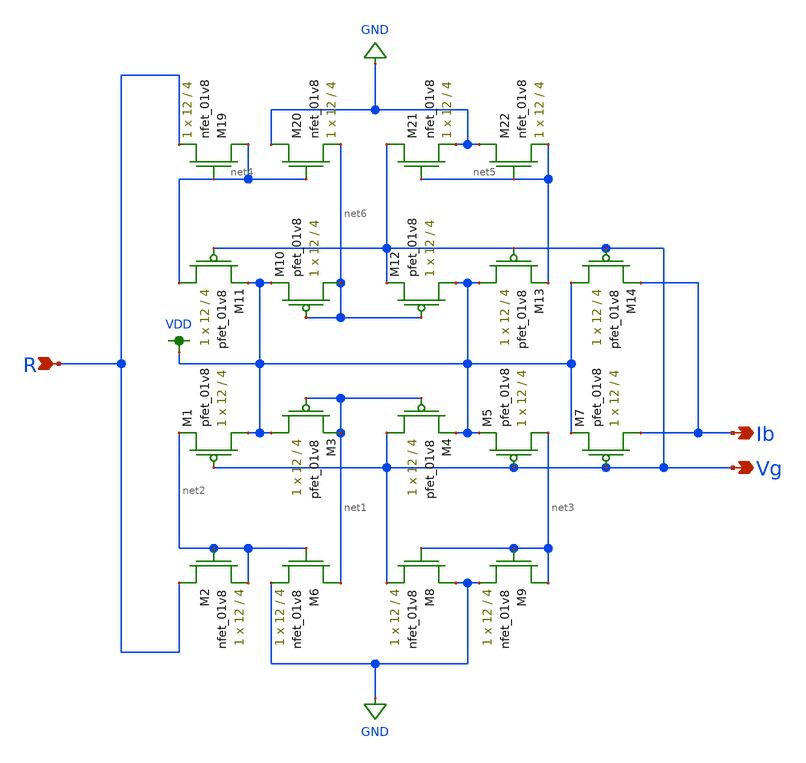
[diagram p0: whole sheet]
** sch_path: modules/bias_gen_lds.sch
**.subckt bias_gen_lds R Ib Vg
*.ipin R
*.opin Ib
*.opin Vg
XM2 R net2 net2 GND sky130_fd_pr__nfet_01v8 L=4 W=12 nf=1 ad='int((nf+1)/2) * W/nf * 0.29' as='int((nf+2)/2) * W/nf * 0.29'
+ pd='2*int((nf+1)/2) * (W/nf + 0.29)' ps='2*int((nf+2)/2) * (W/nf + 0.29)' nrd='0.29 / W' nrs='0.29 / W'
+ sa=0 sb=0 sd=0 mult=1 m=1
XM3 VDD net1 net1 VDD sky130_fd_pr__pfet_01v8 L=4 W=12 nf=1 ad='int((nf+1)/2) * W/nf * 0.29' as='int((nf+2)/2) * W/nf * 0.29'
+ pd='2*int((nf+1)/2) * (W/nf + 0.29)' ps='2*int((nf+2)/2) * (W/nf + 0.29)' nrd='0.29 / W' nrs='0.29 / W'
+ sa=0 sb=0 sd=0 mult=1 m=1
XM1 VDD Vg net2 VDD sky130_fd_pr__pfet_01v8 L=4 W=12 nf=1 ad='int((nf+1)/2) * W/nf * 0.29' as='int((nf+2)/2) * W/nf * 0.29'
+ pd='2*int((nf+1)/2) * (W/nf + 0.29)' ps='2*int((nf+2)/2) * (W/nf + 0.29)' nrd='0.29 / W' nrs='0.29 / W'
+ sa=0 sb=0 sd=0 mult=1 m=1
XM4 Vg net1 VDD VDD sky130_fd_pr__pfet_01v8 L=4 W=12 nf=1 ad='int((nf+1)/2) * W/nf * 0.29' as='int((nf+2)/2) * W/nf * 0.29'
+ pd='2*int((nf+1)/2) * (W/nf + 0.29)' ps='2*int((nf+2)/2) * (W/nf + 0.29)' nrd='0.29 / W' nrs='0.29 / W'
+ sa=0 sb=0 sd=0 mult=1 m=1
XM5 net3 Vg VDD VDD sky130_fd_pr__pfet_01v8 L=4 W=12 nf=1 ad='int((nf+1)/2) * W/nf * 0.29' as='int((nf+2)/2) * W/nf * 0.29'
+ pd='2*int((nf+1)/2) * (W/nf + 0.29)' ps='2*int((nf+2)/2) * (W/nf + 0.29)' nrd='0.29 / W' nrs='0.29 / W'
+ sa=0 sb=0 sd=0 mult=1 m=1
XM7 Ib Vg VDD VDD sky130_fd_pr__pfet_01v8 L=4 W=12 nf=1 ad='int((nf+1)/2) * W/nf * 0.29' as='int((nf+2)/2) * W/nf * 0.29'
+ pd='2*int((nf+1)/2) * (W/nf + 0.29)' ps='2*int((nf+2)/2) * (W/nf + 0.29)' nrd='0.29 / W' nrs='0.29 / W'
+ sa=0 sb=0 sd=0 mult=1 m=1
XM6 net1 net2 GND GND sky130_fd_pr__nfet_01v8 L=4 W=12 nf=1 ad='int((nf+1)/2) * W/nf * 0.29' as='int((nf+2)/2) * W/nf * 0.29'
+ pd='2*int((nf+1)/2) * (W/nf + 0.29)' ps='2*int((nf+2)/2) * (W/nf + 0.29)' nrd='0.29 / W' nrs='0.29 / W'
+ sa=0 sb=0 sd=0 mult=1 m=1
XM8 GND net3 Vg GND sky130_fd_pr__nfet_01v8 L=4 W=12 nf=1 ad='int((nf+1)/2) * W/nf * 0.29' as='int((nf+2)/2) * W/nf * 0.29'
+ pd='2*int((nf+1)/2) * (W/nf + 0.29)' ps='2*int((nf+2)/2) * (W/nf + 0.29)' nrd='0.29 / W' nrs='0.29 / W'
+ sa=0 sb=0 sd=0 mult=1 m=1
XM9 net3 net3 GND GND sky130_fd_pr__nfet_01v8 L=4 W=12 nf=1 ad='int((nf+1)/2) * W/nf * 0.29' as='int((nf+2)/2) * W/nf * 0.29'
+ pd='2*int((nf+1)/2) * (W/nf + 0.29)' ps='2*int((nf+2)/2) * (W/nf + 0.29)' nrd='0.29 / W' nrs='0.29 / W'
+ sa=0 sb=0 sd=0 mult=1 m=1
XM19 net4 net4 R GND sky130_fd_pr__nfet_01v8 L=4 W=12 nf=1 ad='int((nf+1)/2) * W/nf * 0.29' as='int((nf+2)/2) * W/nf * 0.29'
+ pd='2*int((nf+1)/2) * (W/nf + 0.29)' ps='2*int((nf+2)/2) * (W/nf + 0.29)' nrd='0.29 / W' nrs='0.29 / W'
+ sa=0 sb=0 sd=0 mult=1 m=1
XM20 GND net4 net6 GND sky130_fd_pr__nfet_01v8 L=4 W=12 nf=1 ad='int((nf+1)/2) * W/nf * 0.29' as='int((nf+2)/2) * W/nf * 0.29'
+ pd='2*int((nf+1)/2) * (W/nf + 0.29)' ps='2*int((nf+2)/2) * (W/nf + 0.29)' nrd='0.29 / W' nrs='0.29 / W'
+ sa=0 sb=0 sd=0 mult=1 m=1
XM21 Vg net5 GND GND sky130_fd_pr__nfet_01v8 L=4 W=12 nf=1 ad='int((nf+1)/2) * W/nf * 0.29' as='int((nf+2)/2) * W/nf * 0.29'
+ pd='2*int((nf+1)/2) * (W/nf + 0.29)' ps='2*int((nf+2)/2) * (W/nf + 0.29)' nrd='0.29 / W' nrs='0.29 / W'
+ sa=0 sb=0 sd=0 mult=1 m=1
XM22 GND net5 net5 GND sky130_fd_pr__nfet_01v8 L=4 W=12 nf=1 ad='int((nf+1)/2) * W/nf * 0.29' as='int((nf+2)/2) * W/nf * 0.29'
+ pd='2*int((nf+1)/2) * (W/nf + 0.29)' ps='2*int((nf+2)/2) * (W/nf + 0.29)' nrd='0.29 / W' nrs='0.29 / W'
+ sa=0 sb=0 sd=0 mult=1 m=1
XM10 net6 net6 VDD VDD sky130_fd_pr__pfet_01v8 L=4 W=12 nf=1 ad='int((nf+1)/2) * W/nf * 0.29' as='int((nf+2)/2) * W/nf * 0.29'
+ pd='2*int((nf+1)/2) * (W/nf + 0.29)' ps='2*int((nf+2)/2) * (W/nf + 0.29)' nrd='0.29 / W' nrs='0.29 / W'
+ sa=0 sb=0 sd=0 mult=1 m=1
XM11 net4 Vg VDD VDD sky130_fd_pr__pfet_01v8 L=4 W=12 nf=1 ad='int((nf+1)/2) * W/nf * 0.29' as='int((nf+2)/2) * W/nf * 0.29'
+ pd='2*int((nf+1)/2) * (W/nf + 0.29)' ps='2*int((nf+2)/2) * (W/nf + 0.29)' nrd='0.29 / W' nrs='0.29 / W'
+ sa=0 sb=0 sd=0 mult=1 m=1
XM12 VDD net6 Vg VDD sky130_fd_pr__pfet_01v8 L=4 W=12 nf=1 ad='int((nf+1)/2) * W/nf * 0.29' as='int((nf+2)/2) * W/nf * 0.29'
+ pd='2*int((nf+1)/2) * (W/nf + 0.29)' ps='2*int((nf+2)/2) * (W/nf + 0.29)' nrd='0.29 / W' nrs='0.29 / W'
+ sa=0 sb=0 sd=0 mult=1 m=1
XM13 VDD Vg net5 VDD sky130_fd_pr__pfet_01v8 L=4 W=12 nf=1 ad='int((nf+1)/2) * W/nf * 0.29' as='int((nf+2)/2) * W/nf * 0.29'
+ pd='2*int((nf+1)/2) * (W/nf + 0.29)' ps='2*int((nf+2)/2) * (W/nf + 0.29)' nrd='0.29 / W' nrs='0.29 / W'
+ sa=0 sb=0 sd=0 mult=1 m=1
XM14 VDD Vg Ib VDD sky130_fd_pr__pfet_01v8 L=4 W=12 nf=1 ad='int((nf+1)/2) * W/nf * 0.29' as='int((nf+2)/2) * W/nf * 0.29'
+ pd='2*int((nf+1)/2) * (W/nf + 0.29)' ps='2*int((nf+2)/2) * (W/nf + 0.29)' nrd='0.29 / W' nrs='0.29 / W'
+ sa=0 sb=0 sd=0 mult=1 m=1
**.ends
.GLOBAL VDD
.GLOBAL GND
.end
